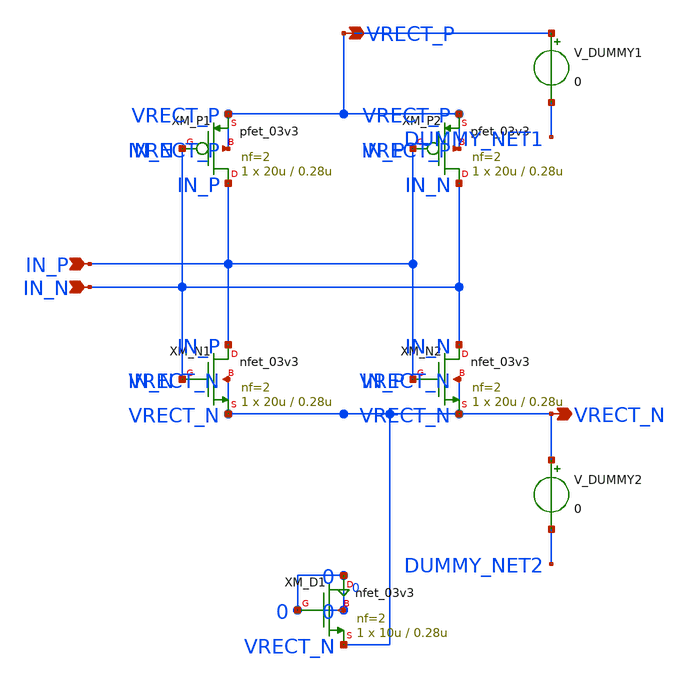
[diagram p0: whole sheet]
** sch_path: modules/PandaChip/designs/iris-harvester/exp/rectifier.sch
**.subckt rectifier IN_P IN_N VRECT_P VRECT_N
*.ipin IN_P
*.ipin IN_N
*.opin VRECT_P
*.opin VRECT_N
XM_P1 IN_P IN_N VRECT_P VRECT_P pfet_03v3 L=0.28u W=20u nf=2 ad='int((nf+1)/2) * W/nf * 0.18u' as='int((nf+2)/2) * W/nf * 0.18u'
+ pd='2*int((nf+1)/2) * (W/nf + 0.18u)' ps='2*int((nf+2)/2) * (W/nf + 0.18u)' nrd='0.18u / W' nrs='0.18u / W'
+ sa=0 sb=0 sd=0 m=1
XM_P2 IN_N IN_P VRECT_P VRECT_P pfet_03v3 L=0.28u W=20u nf=2 ad='int((nf+1)/2) * W/nf * 0.18u' as='int((nf+2)/2) * W/nf * 0.18u'
+ pd='2*int((nf+1)/2) * (W/nf + 0.18u)' ps='2*int((nf+2)/2) * (W/nf + 0.18u)' nrd='0.18u / W' nrs='0.18u / W'
+ sa=0 sb=0 sd=0 m=1
XM_N1 IN_P IN_N VRECT_N VRECT_N nfet_03v3 L=0.28u W=20u nf=2 ad='int((nf+1)/2) * W/nf * 0.18u' as='int((nf+2)/2) * W/nf * 0.18u'
+ pd='2*int((nf+1)/2) * (W/nf + 0.18u)' ps='2*int((nf+2)/2) * (W/nf + 0.18u)' nrd='0.18u / W' nrs='0.18u / W'
+ sa=0 sb=0 sd=0 m=1
XM_N2 IN_N IN_P VRECT_N VRECT_N nfet_03v3 L=0.28u W=20u nf=2 ad='int((nf+1)/2) * W/nf * 0.18u' as='int((nf+2)/2) * W/nf * 0.18u'
+ pd='2*int((nf+1)/2) * (W/nf + 0.18u)' ps='2*int((nf+2)/2) * (W/nf + 0.18u)' nrd='0.18u / W' nrs='0.18u / W'
+ sa=0 sb=0 sd=0 m=1
XM_D1 0 0 VRECT_N 0 nfet_03v3 L=0.28u W=10u nf=2 ad='int((nf+1)/2) * W/nf * 0.18u' as='int((nf+2)/2) * W/nf * 0.18u'
+ pd='2*int((nf+1)/2) * (W/nf + 0.18u)' ps='2*int((nf+2)/2) * (W/nf + 0.18u)' nrd='0.18u / W' nrs='0.18u / W'
+ sa=0 sb=0 sd=0 m=1
V_DUMMY1 VRECT_P DUMMY_NET1 0
V_DUMMY2 VRECT_N DUMMY_NET2 0
**.ends
.end
